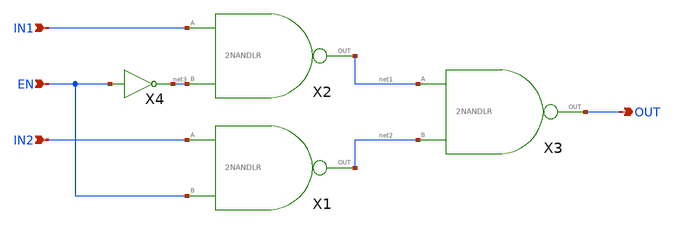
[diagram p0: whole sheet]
** sch_path: task_LATCH/SELECTOR.sch
**.subckt SELECTOR EN IN2 IN1 OUT
*.ipin EN
*.ipin IN2
*.ipin IN1
*.opin OUT
X1 IN2 EN net2 2NANDLR
X2 IN1 net3 net1 2NANDLR
X3 net1 net2 OUT 2NANDLR
X4 EN net3 INVERTER
**.ends

* expanding   symbol:  LR/task_LATCH/2NANDLR.sym # of pins=3
** sym_path: task_LATCH/2NANDLR.sym
** sch_path: task_LATCH/2NANDLR.sch
.subckt 2NANDLR A B OUT
*.ipin A
*.ipin B
*.opin OUT
M1 OUT A net1 GND nch w=3.5u l=3.5u as=0 ps=0 ad=0 pd=0 m=1
M2 OUT B VDD VDD pch w=10.5u l=3.5u as=0 ps=0 ad=0 pd=0 m=1
M3 OUT A VDD VDD pch w=10.5u l=3.5u as=0 ps=0 ad=0 pd=0 m=1
M4 net1 B GND GND nch w=3.5u l=10.5u as=0 ps=0 ad=0 pd=0 m=1
.ends


* expanding   symbol:  LR/task_LATCH/INVERTER.sym # of pins=2
** sym_path: task_LATCH/INVERTER.sym
** sch_path: task_LATCH/INVERTER.sch
.subckt INVERTER IN OUT
*.opin OUT
*.ipin IN
M6 OUT IN VDD VDD pch w=10.5u l=0.35u as=0 ps=0 ad=0 pd=0 m=1
M8 OUT IN GND GND nch w=3.5u l=0.35u as=0 ps=0 ad=0 pd=0 m=1
.ends

.GLOBAL VDD
.GLOBAL GND
.end
